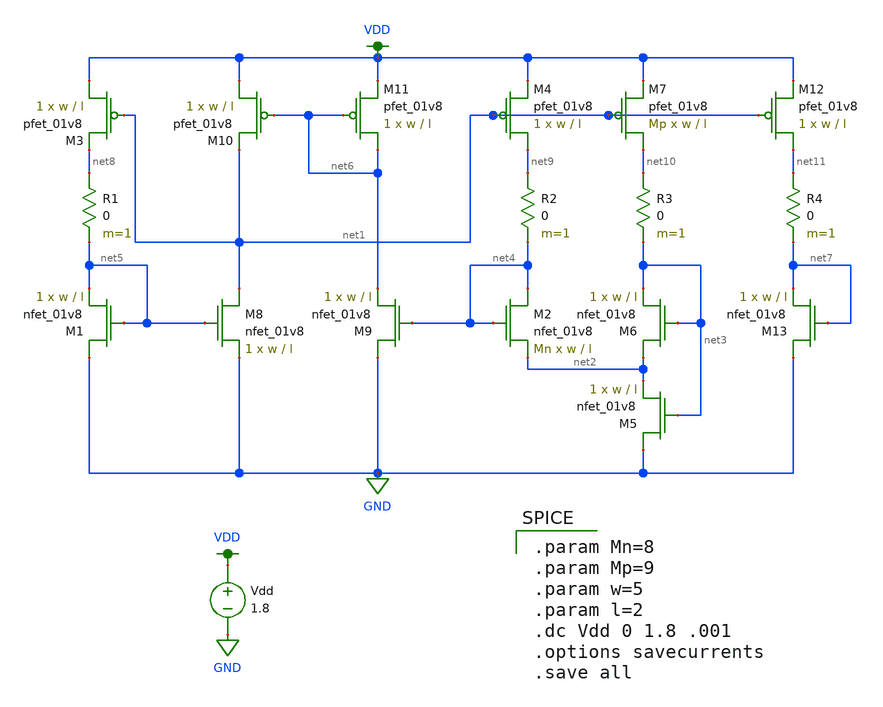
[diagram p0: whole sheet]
** sch_path: biasCurrent - Bryce/magical.sch
**.subckt magical
XM1 GND net5 net5 GND sky130_fd_pr__nfet_01v8 L=l W=w nf=1 ad='int((nf+1)/2) * W/nf * 0.29' as='int((nf+2)/2) * W/nf * 0.29'
+ pd='2*int((nf+1)/2) * (W/nf + 0.29)' ps='2*int((nf+2)/2) * (W/nf + 0.29)' nrd='0.29 / W' nrs='0.29 / W'
+ sa=0 sb=0 sd=0 mult=1 m=1
XM2 net4 net4 net2 GND sky130_fd_pr__nfet_01v8 L=l W=w nf=1 ad='int((nf+1)/2) * W/nf * 0.29' as='int((nf+2)/2) * W/nf * 0.29'
+ pd='2*int((nf+1)/2) * (W/nf + 0.29)' ps='2*int((nf+2)/2) * (W/nf + 0.29)' nrd='0.29 / W' nrs='0.29 / W'
+ sa=0 sb=0 sd=0 mult=Mn m=Mn
XM3 VDD net1 net8 VDD sky130_fd_pr__pfet_01v8 L=l W=w nf=1 ad='int((nf+1)/2) * W/nf * 0.29' as='int((nf+2)/2) * W/nf * 0.29'
+ pd='2*int((nf+1)/2) * (W/nf + 0.29)' ps='2*int((nf+2)/2) * (W/nf + 0.29)' nrd='0.29 / W' nrs='0.29 / W'
+ sa=0 sb=0 sd=0 mult=1 m=1
XM4 net9 net1 VDD VDD sky130_fd_pr__pfet_01v8 L=l W=w nf=1 ad='int((nf+1)/2) * W/nf * 0.29' as='int((nf+2)/2) * W/nf * 0.29'
+ pd='2*int((nf+1)/2) * (W/nf + 0.29)' ps='2*int((nf+2)/2) * (W/nf + 0.29)' nrd='0.29 / W' nrs='0.29 / W'
+ sa=0 sb=0 sd=0 mult=1 m=1
XM5 GND net3 net2 GND sky130_fd_pr__nfet_01v8 L=l W=w nf=1 ad='int((nf+1)/2) * W/nf * 0.29' as='int((nf+2)/2) * W/nf * 0.29'
+ pd='2*int((nf+1)/2) * (W/nf + 0.29)' ps='2*int((nf+2)/2) * (W/nf + 0.29)' nrd='0.29 / W' nrs='0.29 / W'
+ sa=0 sb=0 sd=0 mult=1 m=1
XM6 net2 net3 net3 GND sky130_fd_pr__nfet_01v8 L=l W=w nf=1 ad='int((nf+1)/2) * W/nf * 0.29' as='int((nf+2)/2) * W/nf * 0.29'
+ pd='2*int((nf+1)/2) * (W/nf + 0.29)' ps='2*int((nf+2)/2) * (W/nf + 0.29)' nrd='0.29 / W' nrs='0.29 / W'
+ sa=0 sb=0 sd=0 mult=1 m=1
XM7 net10 net1 VDD VDD sky130_fd_pr__pfet_01v8 L=l W=w nf=1 ad='int((nf+1)/2) * W/nf * 0.29' as='int((nf+2)/2) * W/nf * 0.29'
+ pd='2*int((nf+1)/2) * (W/nf + 0.29)' ps='2*int((nf+2)/2) * (W/nf + 0.29)' nrd='0.29 / W' nrs='0.29 / W'
+ sa=0 sb=0 sd=0 mult=Mp m=Mp
XM8 net1 net5 GND GND sky130_fd_pr__nfet_01v8 L=l W=w nf=1 ad='int((nf+1)/2) * W/nf * 0.29' as='int((nf+2)/2) * W/nf * 0.29'
+ pd='2*int((nf+1)/2) * (W/nf + 0.29)' ps='2*int((nf+2)/2) * (W/nf + 0.29)' nrd='0.29 / W' nrs='0.29 / W'
+ sa=0 sb=0 sd=0 mult=1 m=1
XM9 GND net4 net6 GND sky130_fd_pr__nfet_01v8 L=l W=w nf=1 ad='int((nf+1)/2) * W/nf * 0.29' as='int((nf+2)/2) * W/nf * 0.29'
+ pd='2*int((nf+1)/2) * (W/nf + 0.29)' ps='2*int((nf+2)/2) * (W/nf + 0.29)' nrd='0.29 / W' nrs='0.29 / W'
+ sa=0 sb=0 sd=0 mult=1 m=1
XM10 VDD net6 net1 VDD sky130_fd_pr__pfet_01v8 L=l W=w nf=1 ad='int((nf+1)/2) * W/nf * 0.29' as='int((nf+2)/2) * W/nf * 0.29'
+ pd='2*int((nf+1)/2) * (W/nf + 0.29)' ps='2*int((nf+2)/2) * (W/nf + 0.29)' nrd='0.29 / W' nrs='0.29 / W'
+ sa=0 sb=0 sd=0 mult=1 m=1
XM11 net6 net6 VDD VDD sky130_fd_pr__pfet_01v8 L=l W=w nf=1 ad='int((nf+1)/2) * W/nf * 0.29' as='int((nf+2)/2) * W/nf * 0.29'
+ pd='2*int((nf+1)/2) * (W/nf + 0.29)' ps='2*int((nf+2)/2) * (W/nf + 0.29)' nrd='0.29 / W' nrs='0.29 / W'
+ sa=0 sb=0 sd=0 mult=1 m=1
Vdd VDD GND 1.8
XM12 net11 net1 VDD VDD sky130_fd_pr__pfet_01v8 L=l W=w nf=1 ad='int((nf+1)/2) * W/nf * 0.29' as='int((nf+2)/2) * W/nf * 0.29'
+ pd='2*int((nf+1)/2) * (W/nf + 0.29)' ps='2*int((nf+2)/2) * (W/nf + 0.29)' nrd='0.29 / W' nrs='0.29 / W'
+ sa=0 sb=0 sd=0 mult=1 m=1
XM13 GND net7 net7 GND sky130_fd_pr__nfet_01v8 L=l W=w nf=1 ad='int((nf+1)/2) * W/nf * 0.29' as='int((nf+2)/2) * W/nf * 0.29'
+ pd='2*int((nf+1)/2) * (W/nf + 0.29)' ps='2*int((nf+2)/2) * (W/nf + 0.29)' nrd='0.29 / W' nrs='0.29 / W'
+ sa=0 sb=0 sd=0 mult=1 m=1
R1 net8 net5 0 m=1
R2 net9 net4 0 m=1
R3 net10 net3 0 m=1
R4 net11 net7 0 m=1
**** begin user architecture code

.option wnflag=1
.lib ~/skywater/skywater-pdk/libraries/sky130_fd_pr_ngspice/latest/models/sky130.lib.spice tt


.param Mn=8
.param Mp=9
.param w=5
.param l=2
.dc Vdd 0 1.8 .001
.options savecurrents
.save all

Iout
**** end user architecture code
**.ends
.GLOBAL VDD
.GLOBAL GND
.end
